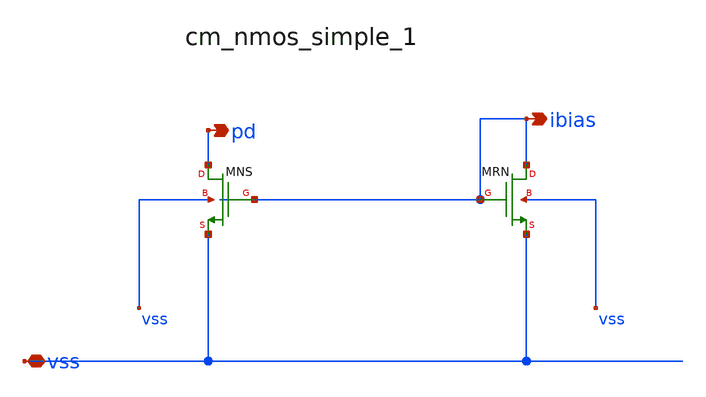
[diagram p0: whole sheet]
** sch_path: analog-db/raw/buf_001_super_follower/hier/blocks/cm_nmos_simple_1.sch
**.subckt cm_nmos_simple_1 vss pd ibias
*.iopin vss
*.opin pd
*.opin ibias
XMNS pd ibias vss vss sg13_lv_nmos w=x_dut_xmns_w l=x_dut_xmns_l ng=1 m=x_dut_xmns_m
XMRN ibias ibias vss vss sg13_lv_nmos w=x_dut_xmrn_w l=x_dut_xmrn_l ng=1 m=x_dut_xmrn_m
**.ends
.end
